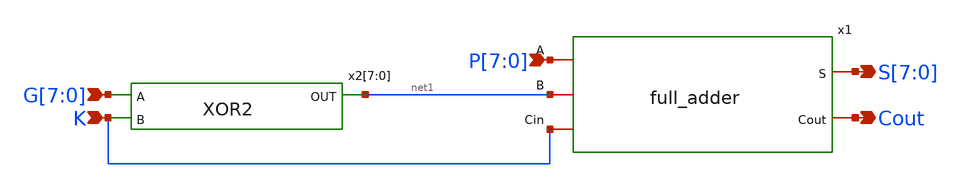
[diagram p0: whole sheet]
** sch_path: design/xschem/SUBTRACTOR/subtractor.sch
**.subckt subtractor P[7],P[6],P[5],P[4],P[3],P[2],P[1],P[0] G[7],G[6],G[5],G[4],G[3],G[2],G[1],G[0]
*+ S[7],S[6],S[5],S[4],S[3],S[2],S[1],S[0] Cout K
*.ipin P[7],P[6],P[5],P[4],P[3],P[2],P[1],P[0]
*.ipin G[7],G[6],G[5],G[4],G[3],G[2],G[1],G[0]
*.opin S[7],S[6],S[5],S[4],S[3],S[2],S[1],S[0]
*.opin Cout
*.ipin K
x1 P[7] S[7] net1 K Cout full_adder
x2[7] G[7] K net1 XOR2
x2[6] G[6] K net1 XOR2
x2[5] G[5] K net1 XOR2
x2[4] G[4] K net1 XOR2
x2[3] G[3] K net1 XOR2
x2[2] G[2] K net1 XOR2
x2[1] G[1] K net1 XOR2
x2[0] G[0] K net1 XOR2
**.ends
.end
